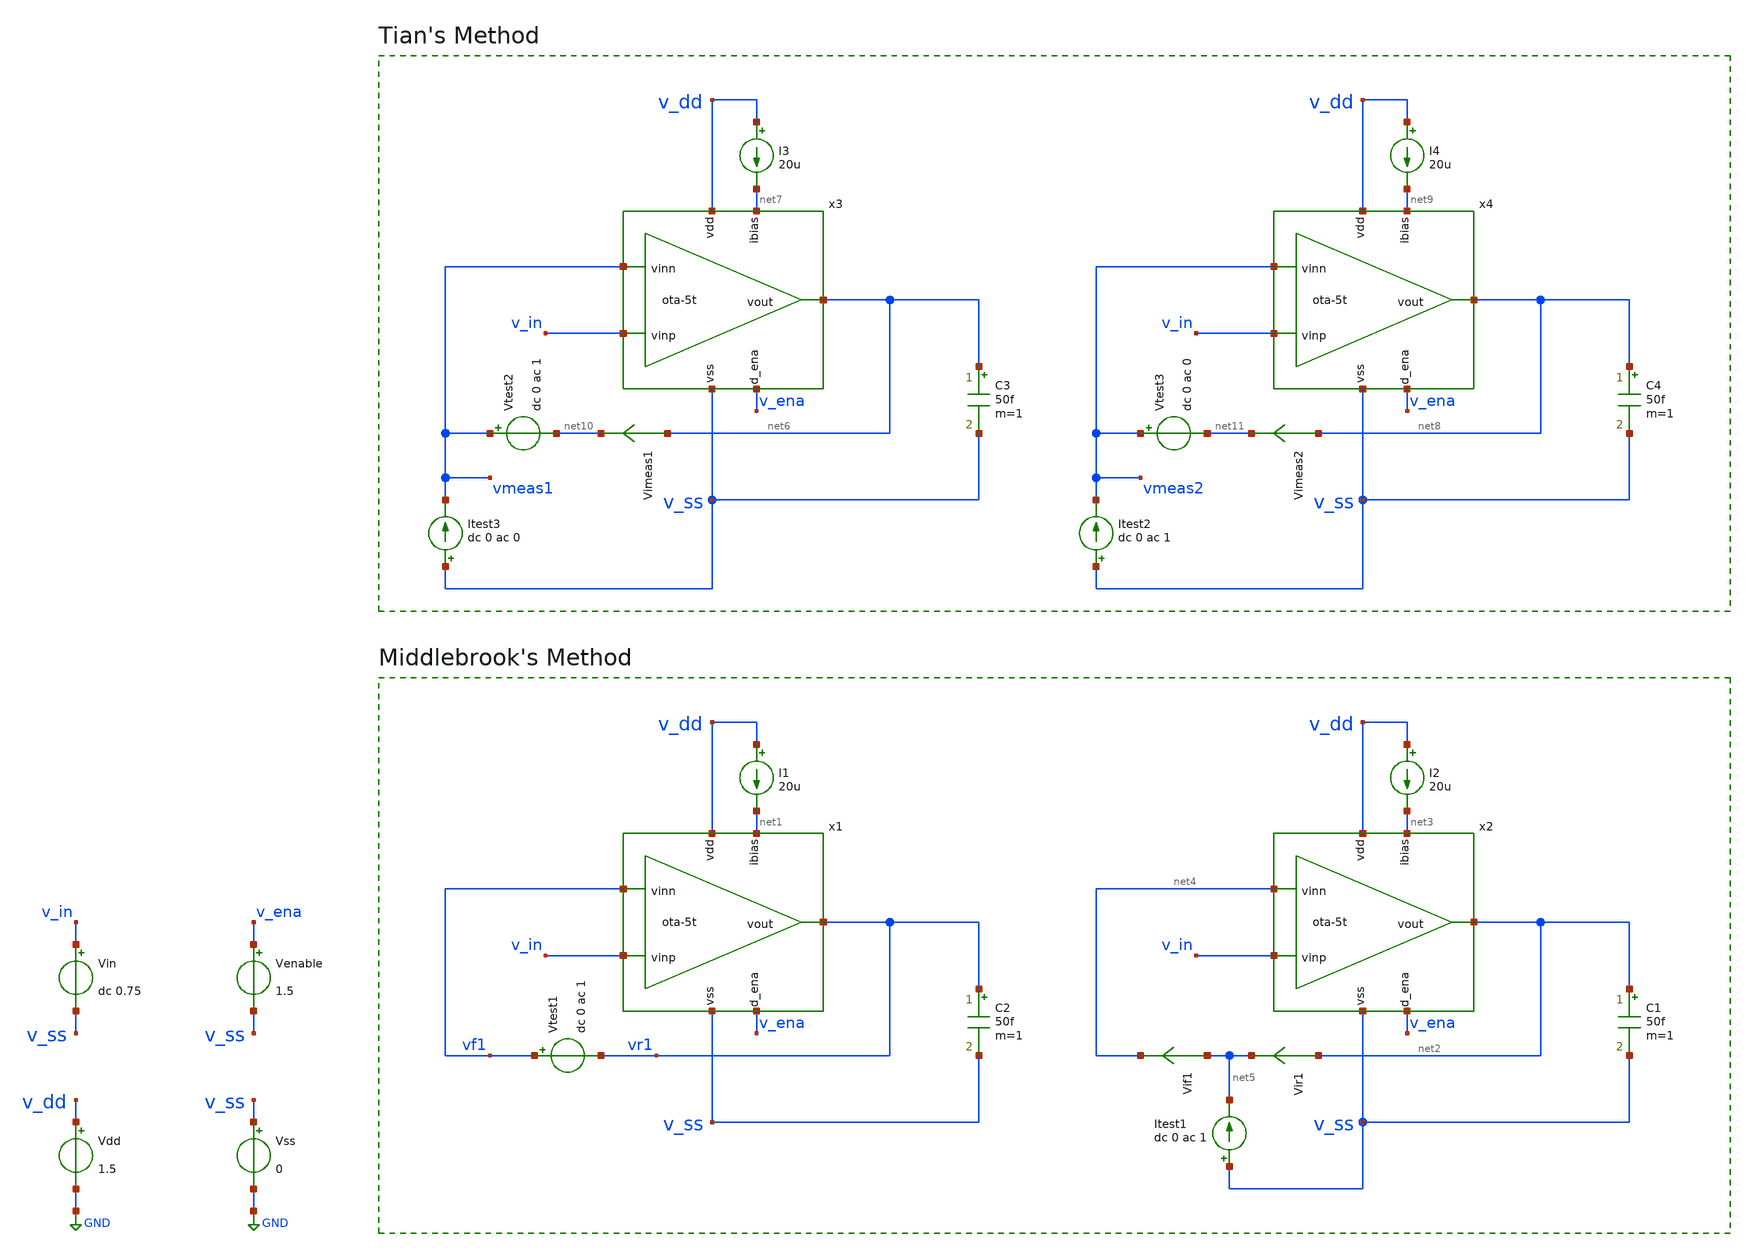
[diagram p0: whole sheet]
** sch_path: prj/template/3_Real_circuits/ota-5t_tb-loopgain.sch
* (c) 2024 H. Pretl, S. Dorrer, Apache-2.0 license
* prj/template/3_Real_circuits/ota-5t.sch:
* (c) 2024-2025 H. Pretl, Apache-2.0 license
**.subckt ota-5t_tb-loopgain
Vdd v_dd GND 1.5
Vss v_ss GND 0
Vin v_in v_ss dc 0.75
Venable v_ena v_ss 1.5
C2 vr1 v_ss 50f m=1
I1 v_dd net1 20u
x1 v_dd vr1 vf1 v_in net1 v_ena v_ss ota-5t
Vtest1 vf1 vr1 dc 0 ac 1
C1 net2 v_ss 50f m=1
I2 v_dd net3 20u
x2 v_dd net2 net4 v_in net3 v_ena v_ss ota-5t
Vir1 net2 net5 0
.save i(vir1)
Vif1 net5 net4 0
.save i(vif1)
Itest1 v_ss net5 dc 0 ac 1
C3 net6 v_ss 50f m=1
I3 v_dd net7 20u
x3 v_dd net6 vmeas1 v_in net7 v_ena v_ss ota-5t
C4 net8 v_ss 50f m=1
I4 v_dd net9 20u
x4 v_dd net8 vmeas2 v_in net9 v_ena v_ss ota-5t
Itest3 v_ss vmeas1 dc 0 ac 0
Vtest2 vmeas1 net10 dc 0 ac 1
Vimeas1 net6 net10 0
.save i(vimeas1)
Itest2 v_ss vmeas2 dc 0 ac 1
Vtest3 vmeas2 net11 dc 0 ac 0
Vimeas2 net8 net11 0
.save i(vimeas2)
**** begin user architecture code
 .lib cornerMOSlv.lib mos_tt



.param temp=27
.options savecurrents reltol=1e-3 abstol=1e-12 gmin=1e-15
.control
save all

* Operating Point Analysis
op
remzerovec
write ota-5t_tb-loopgain.raw
set appendwrite

* AC Analysis
ac dec 101 1 100G
remzerovec
write ota-5t_tb-loopgain.raw
set appendwrite

* Middlebrook's Method
let tv=-v(vr1)/v(vf1)
let ti=-i(vir1)/i(vif1)
let tmb=(tv*ti - 1)/(tv + ti + 2)

plot db(tmb) ylabel 'Magnitude - Middlebrook'
plot 180/pi*cphase(tmb) ylabel 'Phase - Middlebrook'

* Tian's Method
* vtest=0, itest=1:
let A=i(Vimeas2)
let C=v(vmeas2)

* vtest=1, itest=0:
let B=i(Vimeas1)
let D=v(vmeas1)
let ttian=(A*D-B*C-A)/(2*(B*C-A*D)+A-D+1)

plot db(ttian) ylabel 'Magnitude - Tian'
plot 180/pi*cphase(ttian) ylabel 'Phase - Tian'

* Middlebrook vs. Tian
plot db(tmb) db(ttian) ylabel 'Magnitude'
plot 180/pi*cphase(tmb) 180/pi*cphase(ttian) ylabel 'Phase'

write ota-5t_tb-loopgain.raw

*quit
.endc


**** end user architecture code
**.ends

* expanding   symbol:  ota-5t.sym # of pins=7
** sym_path: prj/template/3_Real_circuits/ota-5t.sym
** sch_path: prj/template/3_Real_circuits/ota-5t.sch
.subckt ota-5t vdd vout vinn vinp ibias d_ena vss
*.ipin ibias
*.iopin vdd
*.iopin vss
*.ipin vinp
*.ipin vinn
*.opin vout
*.ipin d_ena
XM5 tail gate_n vss vss sg13_lv_nmos w=0.5u l=5u ng=1 m=1 mm_ok=1
XM4 vout gate_p vdd vdd sg13_lv_pmos w=1.5u l=5u ng=1 m=1 mm_ok=1
XM1 gate_p vinp tail vss sg13_lv_nmos w=2u l=5u ng=1 m=1 mm_ok=1
XM2 vout vinn tail vss sg13_lv_nmos w=2u l=5u ng=1 m=1 mm_ok=1
XM3 gate_p gate_p vdd vdd sg13_lv_pmos w=1.5u l=5u ng=1 m=1 mm_ok=1
XM6 ibias gate_n vss vss sg13_lv_nmos w=2.5u l=5u ng=5 m=1 mm_ok=1
XM9 gate_n ena_n vss vss sg13_lv_nmos w=0.5u l=0.13u ng=1 m=1 mm_ok=1
XM11 gate_p ena vdd vdd sg13_lv_pmos w=1.5u l=0.13u ng=1 m=1 mm_ok=1
XM7 ena ena_n vss vss sg13_lv_nmos w=0.5u l=0.13u ng=1 m=1 mm_ok=1
XM8 ena ena_n vdd vdd sg13_lv_pmos w=1.5u l=0.13u ng=1 m=1 mm_ok=1
XM10 ibias ena gate_n vss sg13_lv_nmos w=0.5u l=0.13u ng=1 m=1 mm_ok=1
XM12 ena_n d_ena vss vss sg13_lv_nmos w=0.5u l=0.13u ng=1 m=1 mm_ok=1
XM13 ena_n d_ena vdd vdd sg13_lv_pmos w=1.5u l=0.13u ng=1 m=1 mm_ok=1
.ends

.GLOBAL GND
.end
